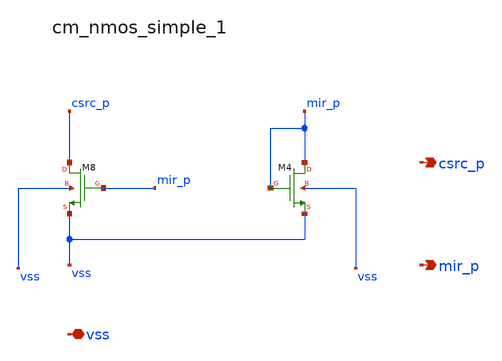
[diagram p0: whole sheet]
** sch_path: analog-db/raw/amp_025_hsu_classab_ota/hier/blocks/cm_nmos_simple_1.sch
**.subckt cm_nmos_simple_1 vss csrc_p mir_p
*.iopin vss
*.opin csrc_p
*.opin mir_p
XM4 mir_p mir_p vss vss sg13_lv_nmos w=x_dut_xm4_w l=x_dut_xm4_l ng=1 m=x_dut_xm4_m
XM8 csrc_p mir_p vss vss sg13_lv_nmos w=x_dut_xm8_w l=x_dut_xm8_l ng=1 m=x_dut_xm8_m
**.ends
.end
